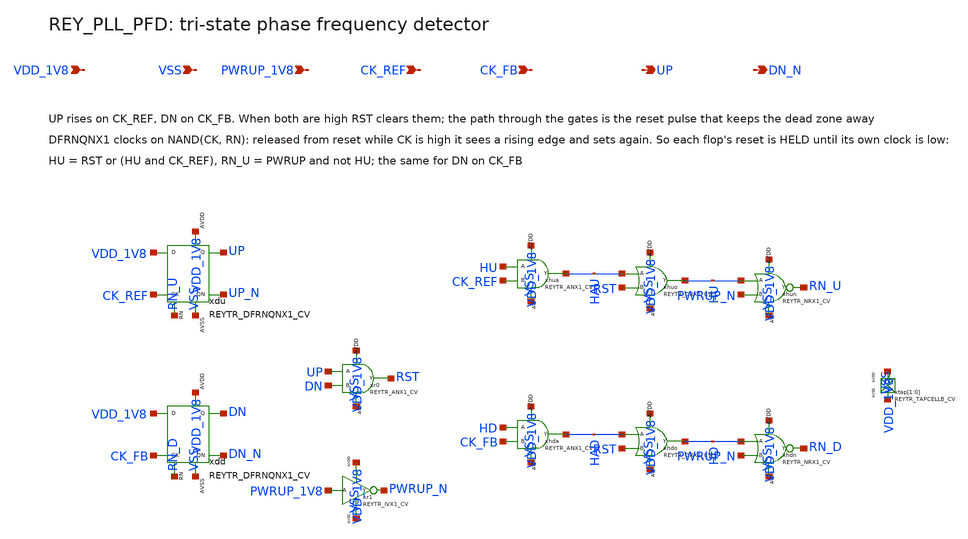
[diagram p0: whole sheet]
** sch_path: design/REY_PLL_SKY130A/REY_PLL_PFD.sch
**.subckt REY_PLL_PFD VDD_1V8 VSS PWRUP_1V8 CK_REF CK_FB UP DN_N
*.ipin VDD_1V8
*.ipin VSS
*.ipin PWRUP_1V8
*.ipin CK_REF
*.ipin CK_FB
*.opin UP
*.opin DN_N
xdu VDD_1V8 CK_REF RN_U UP UP_N VDD_1V8 VSS REYTR_DFRNQNX1_CV xoffset=0 yoffset=0 angle=0
xdd VDD_1V8 CK_FB RN_D DN DN_N VDD_1V8 VSS REYTR_DFRNQNX1_CV xoffset=0 yoffset=0 angle=0
xr0 UP DN RST VDD_1V8 VSS REYTR_ANX1_CV xoffset=0 yoffset=0 angle=0 M=1
xr1 PWRUP_1V8 PWRUP_N VDD_1V8 VSS REYTR_IVX1_CV
xhua HU CK_REF HAU VDD_1V8 VSS REYTR_ANX1_CV xoffset=0 yoffset=0 angle=0 M=1
xhuo HAU RST HU VDD_1V8 VSS REYTR_ORX1_CV xoffset=0 yoffset=0 angle=0 M=1
xhun HU PWRUP_N RN_U VDD_1V8 VSS REYTR_NRX1_CV
xhda HD CK_FB HAD VDD_1V8 VSS REYTR_ANX1_CV xoffset=0 yoffset=0 angle=0 M=1
xhdo HAD RST HD VDD_1V8 VSS REYTR_ORX1_CV xoffset=0 yoffset=0 angle=0 M=1
xhdn HD PWRUP_N RN_D VDD_1V8 VSS REYTR_NRX1_CV
xtap[1] VDD_1V8 VSS REYTR_TAPCELLB_CV xoffset=0 yoffset=0 angle=0
xtap[0] VDD_1V8 VSS REYTR_TAPCELLB_CV xoffset=0 yoffset=0 angle=0
**.ends
.end
